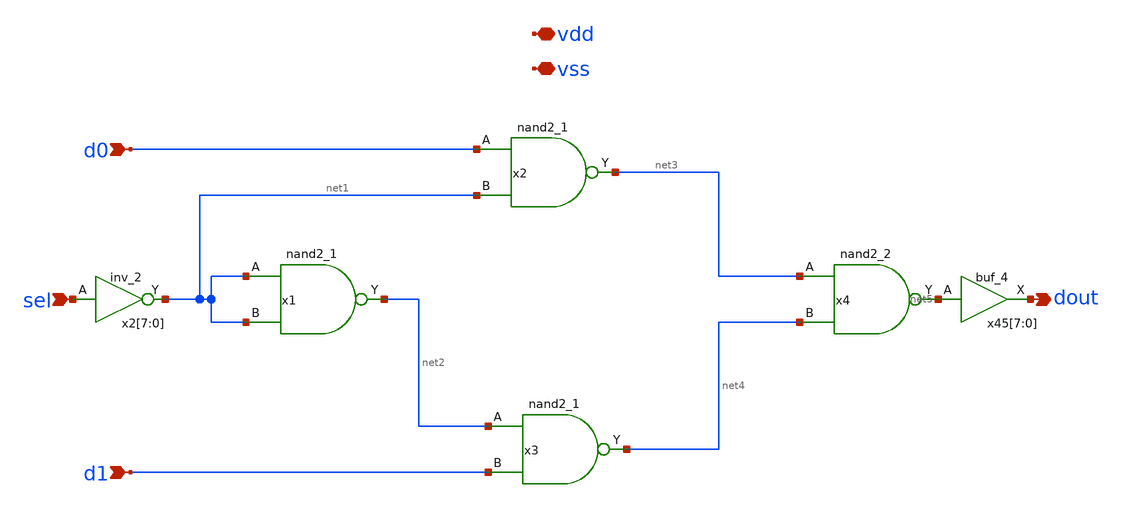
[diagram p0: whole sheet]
** sch_path: top/test/design/mux2to1.sch
**.subckt mux2to1 vss vdd d0 sel d1 dout
*.iopin vss
*.iopin vdd
*.ipin d0
*.ipin sel
*.ipin d1
*.opin dout
x1 net1 net1 vss vss vdd vdd net2 sky130_fd_sc_hd__nand2_1
x2 d0 net1 vss vss vdd vdd net3 sky130_fd_sc_hd__nand2_1
x3 net2 d1 vss vss vdd vdd net4 sky130_fd_sc_hd__nand2_1
x4 net3 net4 vss vss vdd vdd net5 sky130_fd_sc_hd__nand2_2
x45[7] net5 vss vss vdd vdd dout sky130_fd_sc_hd__buf_4
x45[6] net5 vss vss vdd vdd dout sky130_fd_sc_hd__buf_4
x45[5] net5 vss vss vdd vdd dout sky130_fd_sc_hd__buf_4
x45[4] net5 vss vss vdd vdd dout sky130_fd_sc_hd__buf_4
x45[3] net5 vss vss vdd vdd dout sky130_fd_sc_hd__buf_4
x45[2] net5 vss vss vdd vdd dout sky130_fd_sc_hd__buf_4
x45[1] net5 vss vss vdd vdd dout sky130_fd_sc_hd__buf_4
x45[0] net5 vss vss vdd vdd dout sky130_fd_sc_hd__buf_4
x2[7] sel vss vss vdd vdd net1 sky130_fd_sc_hd__inv_2
x2[6] sel vss vss vdd vdd net1 sky130_fd_sc_hd__inv_2
x2[5] sel vss vss vdd vdd net1 sky130_fd_sc_hd__inv_2
x2[4] sel vss vss vdd vdd net1 sky130_fd_sc_hd__inv_2
x2[3] sel vss vss vdd vdd net1 sky130_fd_sc_hd__inv_2
x2[2] sel vss vss vdd vdd net1 sky130_fd_sc_hd__inv_2
x2[1] sel vss vss vdd vdd net1 sky130_fd_sc_hd__inv_2
x2[0] sel vss vss vdd vdd net1 sky130_fd_sc_hd__inv_2
**.ends
.end
